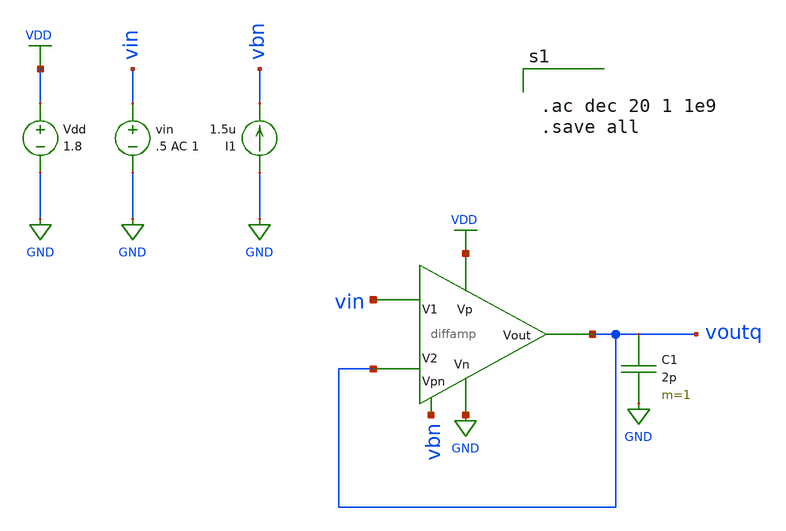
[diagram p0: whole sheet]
** sch_path: mini_proj_3/schematic/diff_2d.sch
**.subckt diff_2d
Vdd VDD GND 1.8
vin vin GND .5 AC 1
I1 GND vbn 1.5u
C1 voutq GND 2p m=1
X1 vbn VDD GND vin voutq voutq diffamp
**** begin user architecture code

.option wnflag=1
.lib ~/skywater/skywater-pdk/libraries/sky130_fd_pr_ngspice/latest/models/sky130.lib.spice tt



.ac dec 20 1 1e9
.save all


**** end user architecture code
**.ends
.GLOBAL VDD
.GLOBAL GND
.end
